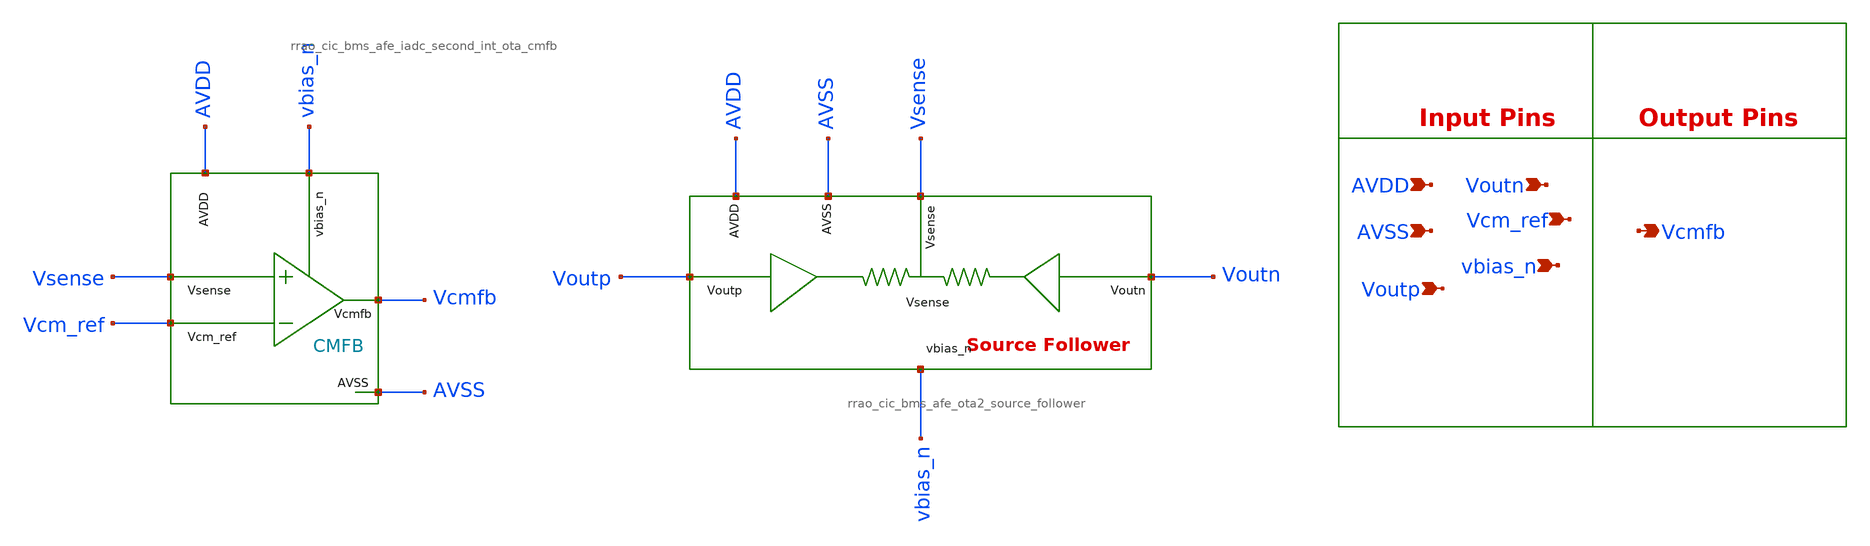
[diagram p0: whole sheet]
** sch_path: design/schematics/ADC/DSM_Loop_filter/Third_int/OTA_Files/rrao_cic_bms_afe_ota2_cmfb_with_sf.sch
**.subckt rrao_cic_bms_afe_ota2_cmfb_with_sf Vcm_ref Voutp Voutn AVDD AVSS vbias_n Vcmfb
*.ipin Vcm_ref
*.ipin Voutp
*.ipin Voutn
*.ipin AVDD
*.ipin AVSS
*.ipin vbias_n
*.opin Vcmfb
x1 AVDD vbias_n AVSS Vcmfb Vcm_ref Vsense rrao_cic_bms_afe_iadc_second_int_ota_cmfb
x2 Voutn AVDD Vsense AVSS vbias_n Voutp rrao_cic_bms_afe_ota2_source_follower
**.ends
.end
